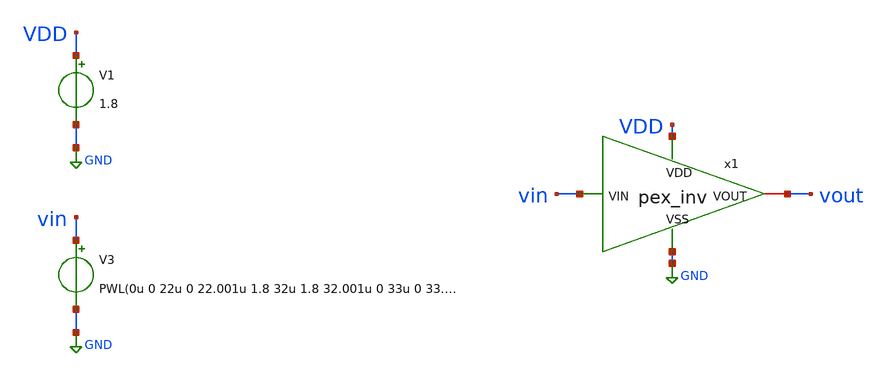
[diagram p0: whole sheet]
** sch_path: schem/tb/tb_inv.sch
**.subckt tb_inv
V1 VDD GND 1.8
V3 vin GND PWL(0u 0 22u 0 22.001u 1.8 32u 1.8 32.001u 0 33u 0 33.001u 1.8 43u 1.8 43.001u 0 44u 0)
x1 VDD vin vout GND inv_1
**** begin user architecture code


.include /home/zhixuan/projects/fyp_vco/magic/ip/inv_1/inv_1.spice
.lib /usr/local/share/pdk/sky130A/libs.tech/ngspice/sky130.lib.spice tt

.tran 10n 45u
.save all

.control
    run
    plot vin vout
.endc

.end


**** end user architecture code
**.ends
.GLOBAL GND
.end
